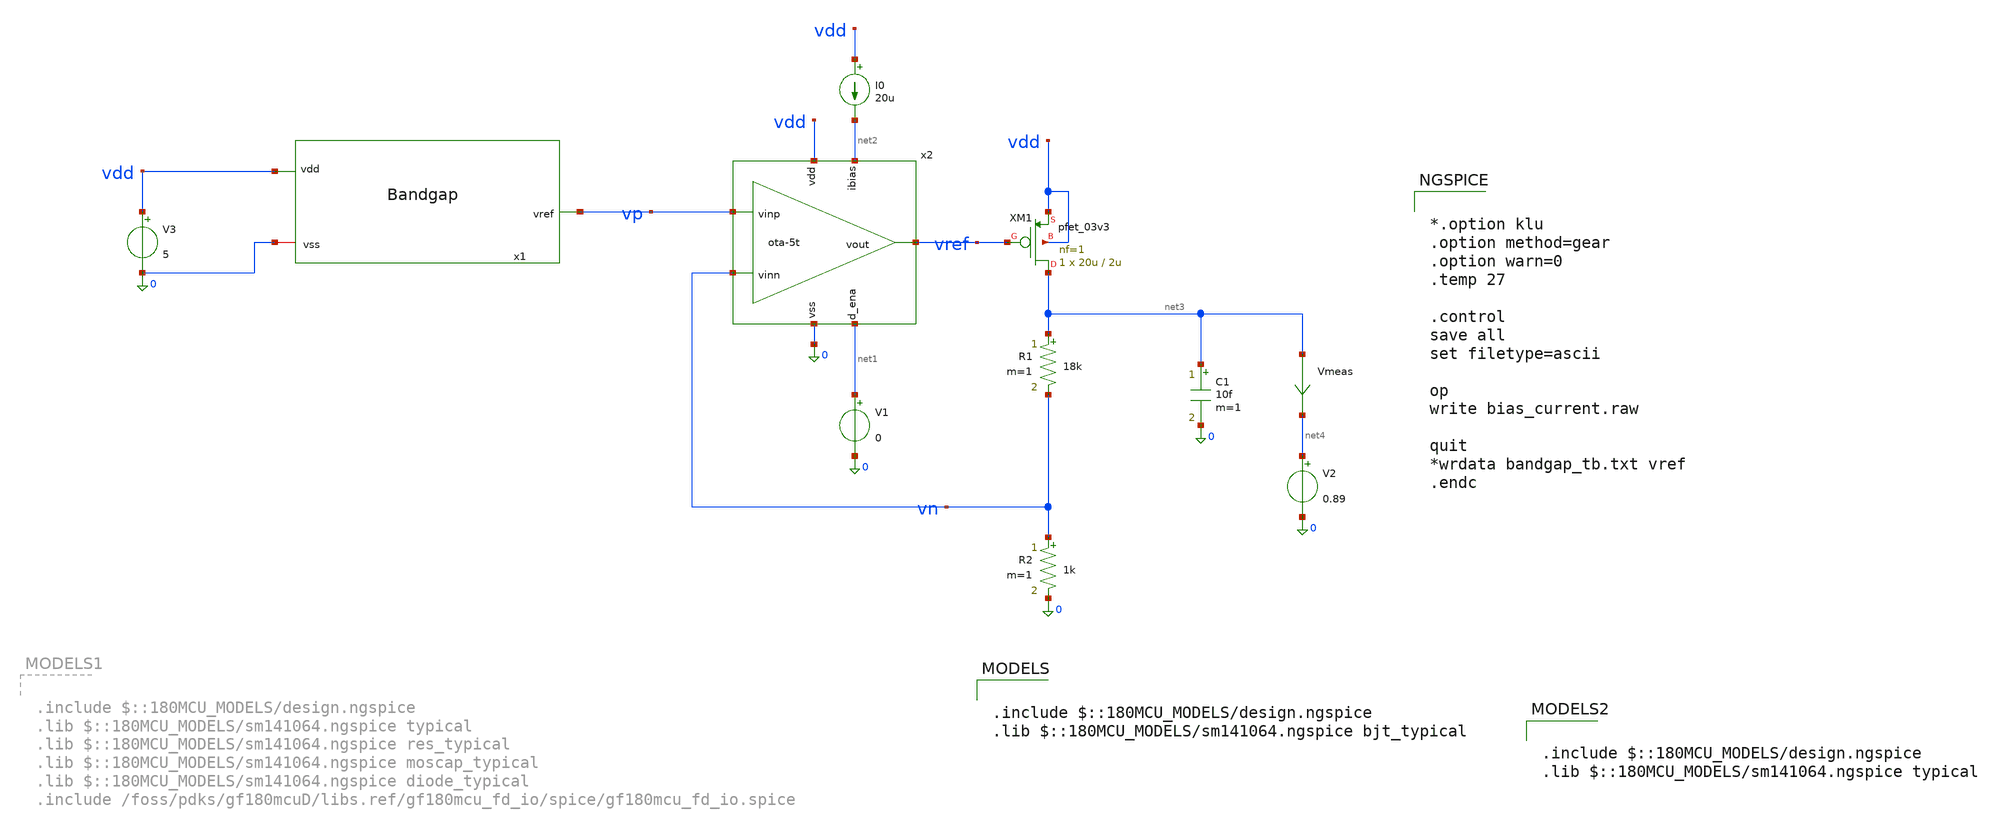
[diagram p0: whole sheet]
** sch_path: xschem/bias_current.sch
**.subckt bias_current
x1 vdd vp 0 bandgap
x2 vdd vref vp vn net2 net1 0 ota-5t
V3 vdd 0 5
V1 net1 0 0
I0 vdd net2 20u
XM1 net3 vref vdd vdd pfet_03v3 L=2u W=20u nf=1 ad='int((nf+1)/2) * W/nf * 0.18u' as='int((nf+2)/2) * W/nf * 0.18u'
+ pd='2*int((nf+1)/2) * (W/nf + 0.18u)' ps='2*int((nf+2)/2) * (W/nf + 0.18u)' nrd='0.18u / W' nrs='0.18u / W'
+ sa=0 sb=0 sd=0 m=1
R1 net3 vn 18k m=1
R2 vn 0 1k m=1
C1 net3 0 10f m=1
Vmeas net3 net4 0
.save i(vmeas)
V2 net4 0 0.89
**** begin user architecture code

.include $::180MCU_MODELS/design.ngspice
.lib $::180MCU_MODELS/sm141064.ngspice bjt_typical



.include $::180MCU_MODELS/design.ngspice
.lib $::180MCU_MODELS/sm141064.ngspice typical



*.option klu
.option method=gear
.option warn=0
.temp 27

.control
save all
set filetype=ascii

op
write bias_current.raw

quit
*wrdata bandgap_tb.txt vref
.endc


**** end user architecture code
**.ends
.end
